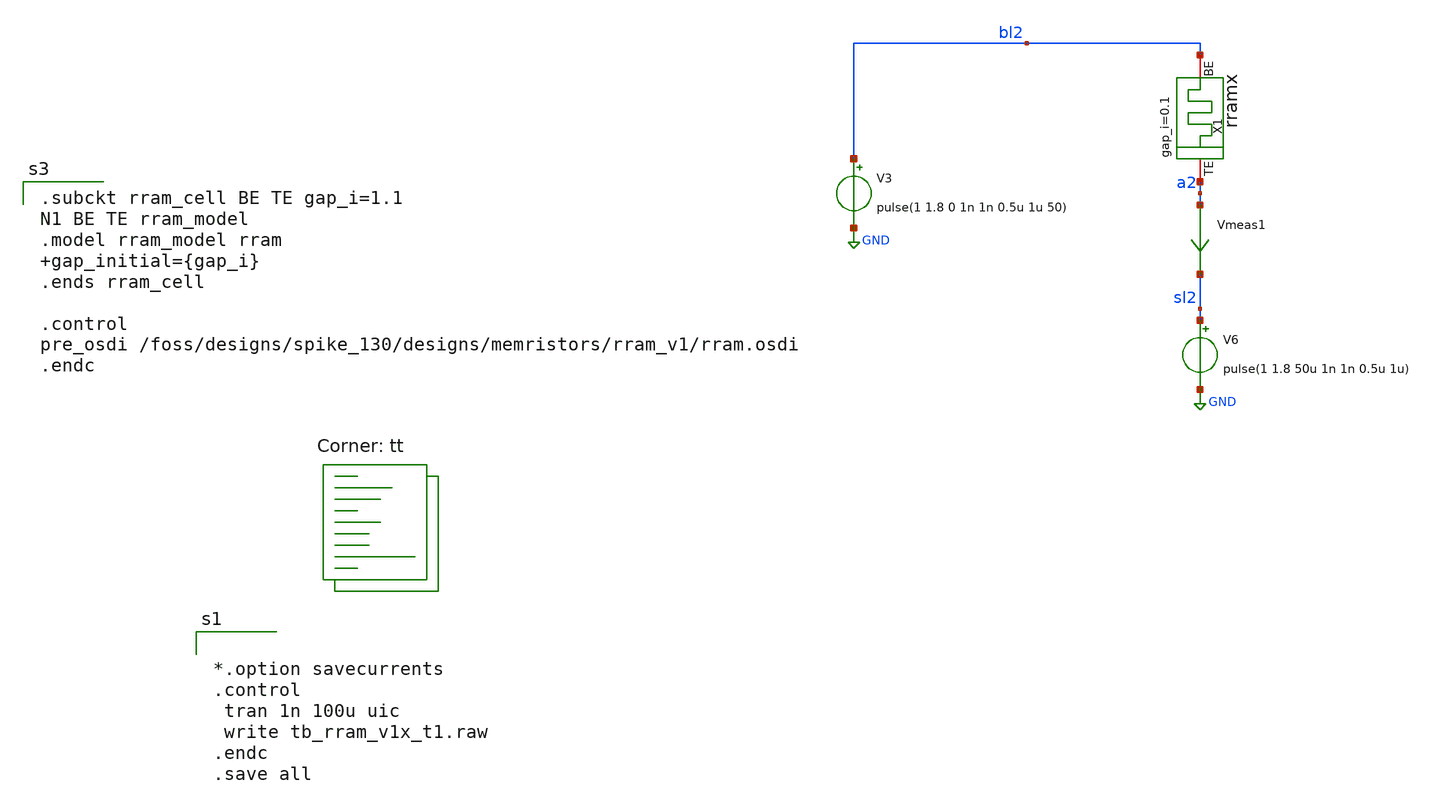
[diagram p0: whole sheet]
** sch_path: designs/tb_memristor/tb_rram_v1x_t1.sch
**.subckt tb_rram_v1x_t1
V3 bl2 GND pulse(1 1.8 0 1n 1n 0.5u 1u 50)
V6 sl2 GND pulse(1 1.8 50u 1n 1n 0.5u 1u)
Vmeas1 a2 sl2 0
.save i(vmeas1)
X1 a2 bl2 rram_cell gap_i=0.1
**** begin user architecture code
.lib $::SKYWATER_MODELS/sky130.lib.spice tt


*.option savecurrents
.control
 tran 1n 100u uic
 write tb_rram_v1x_t1.raw
.endc
.save all


.subckt rram_cell BE TE gap_i=1.1
N1 BE TE rram_model
.model rram_model rram gap_initial={gap_i}
.ends rram_cell

.control
pre_osdi /foss/designs/spike_130/designs/memristors/rram_v1/rram.osdi
.endc

**** end user architecture code
**.ends
.GLOBAL GND
.end
